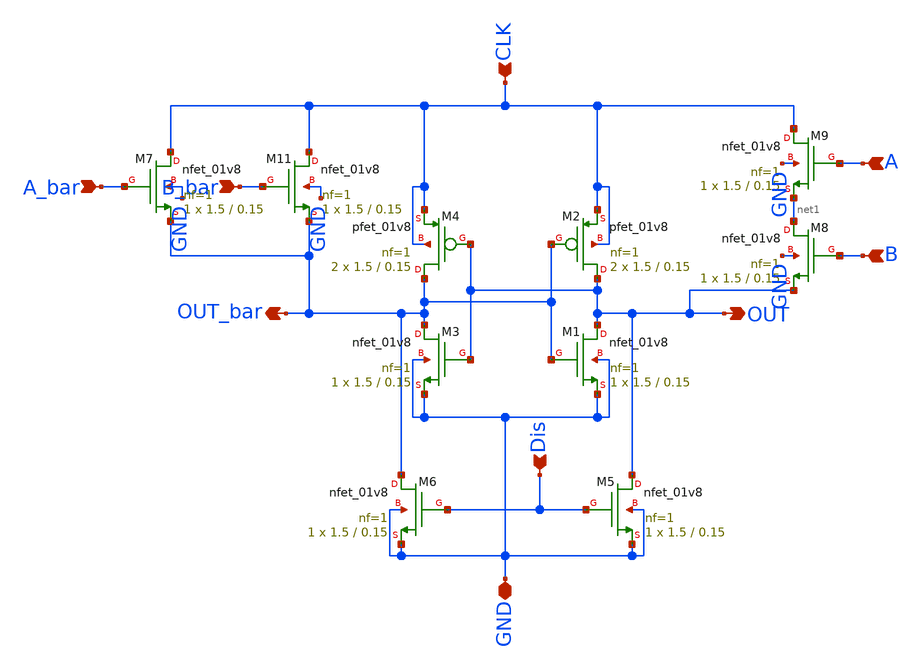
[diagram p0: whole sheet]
** sch_path: skywater_stuff/EESPFAL_NAND_v3_magic_checked.sch
**.subckt EESPFAL_NAND_v3_magic_checked A A_bar B B_bar OUT OUT_bar Dis GND CLK
*.ipin A
*.ipin A_bar
*.ipin B
*.ipin B_bar
*.opin OUT
*.opin OUT_bar
*.ipin Dis
*.iopin GND
*.ipin CLK
XM6 OUT_bar Dis GND GND sky130_fd_pr__nfet_01v8 L=0.15 W=1.5 nf=1 ad='int((nf+1)/2) * W/nf * 0.29' as='int((nf+2)/2) * W/nf * 0.29'
+ pd='2*int((nf+1)/2) * (W/nf + 0.29)' ps='2*int((nf+2)/2) * (W/nf + 0.29)' nrd='0.29 / W' nrs='0.29 / W'
+ sa=0 sb=0 sd=0 mult=1 m=1
XM9 CLK A net1 GND sky130_fd_pr__nfet_01v8 L=0.15 W=1.5 nf=1 ad='int((nf+1)/2) * W/nf * 0.29' as='int((nf+2)/2) * W/nf * 0.29'
+ pd='2*int((nf+1)/2) * (W/nf + 0.29)' ps='2*int((nf+2)/2) * (W/nf + 0.29)' nrd='0.29 / W' nrs='0.29 / W'
+ sa=0 sb=0 sd=0 mult=1 m=1
XM4 OUT_bar OUT CLK CLK sky130_fd_pr__pfet_01v8 L=0.15 W=1.5 nf=1 ad='int((nf+1)/2) * W/nf * 0.29' as='int((nf+2)/2) * W/nf * 0.29'
+ pd='2*int((nf+1)/2) * (W/nf + 0.29)' ps='2*int((nf+2)/2) * (W/nf + 0.29)' nrd='0.29 / W' nrs='0.29 / W'
+ sa=0 sb=0 sd=0 mult=2 m=2
XM3 OUT_bar OUT GND GND sky130_fd_pr__nfet_01v8 L=0.15 W=1.5 nf=1 ad='int((nf+1)/2) * W/nf * 0.29' as='int((nf+2)/2) * W/nf * 0.29'
+ pd='2*int((nf+1)/2) * (W/nf + 0.29)' ps='2*int((nf+2)/2) * (W/nf + 0.29)' nrd='0.29 / W' nrs='0.29 / W'
+ sa=0 sb=0 sd=0 mult=1 m=1
XM2 OUT OUT_bar CLK CLK sky130_fd_pr__pfet_01v8 L=0.15 W=1.5 nf=1 ad='int((nf+1)/2) * W/nf * 0.29' as='int((nf+2)/2) * W/nf * 0.29'
+ pd='2*int((nf+1)/2) * (W/nf + 0.29)' ps='2*int((nf+2)/2) * (W/nf + 0.29)' nrd='0.29 / W' nrs='0.29 / W'
+ sa=0 sb=0 sd=0 mult=2 m=2
XM11 CLK B_bar OUT_bar GND sky130_fd_pr__nfet_01v8 L=0.15 W=1.5 nf=1 ad='int((nf+1)/2) * W/nf * 0.29'
+ as='int((nf+2)/2) * W/nf * 0.29' pd='2*int((nf+1)/2) * (W/nf + 0.29)' ps='2*int((nf+2)/2) * (W/nf + 0.29)'
+ nrd='0.29 / W' nrs='0.29 / W' sa=0 sb=0 sd=0 mult=1 m=1
XM7 CLK A_bar OUT_bar GND sky130_fd_pr__nfet_01v8 L=0.15 W=1.5 nf=1 ad='int((nf+1)/2) * W/nf * 0.29'
+ as='int((nf+2)/2) * W/nf * 0.29' pd='2*int((nf+1)/2) * (W/nf + 0.29)' ps='2*int((nf+2)/2) * (W/nf + 0.29)'
+ nrd='0.29 / W' nrs='0.29 / W' sa=0 sb=0 sd=0 mult=1 m=1
XM8 net1 B OUT GND sky130_fd_pr__nfet_01v8 L=0.15 W=1.5 nf=1 ad='int((nf+1)/2) * W/nf * 0.29' as='int((nf+2)/2) * W/nf * 0.29'
+ pd='2*int((nf+1)/2) * (W/nf + 0.29)' ps='2*int((nf+2)/2) * (W/nf + 0.29)' nrd='0.29 / W' nrs='0.29 / W'
+ sa=0 sb=0 sd=0 mult=1 m=1
XM1 OUT OUT_bar GND GND sky130_fd_pr__nfet_01v8 L=0.15 W=1.5 nf=1 ad='int((nf+1)/2) * W/nf * 0.29' as='int((nf+2)/2) * W/nf * 0.29'
+ pd='2*int((nf+1)/2) * (W/nf + 0.29)' ps='2*int((nf+2)/2) * (W/nf + 0.29)' nrd='0.29 / W' nrs='0.29 / W'
+ sa=0 sb=0 sd=0 mult=1 m=1
XM5 OUT Dis GND GND sky130_fd_pr__nfet_01v8 L=0.15 W=1.5 nf=1 ad='int((nf+1)/2) * W/nf * 0.29' as='int((nf+2)/2) * W/nf * 0.29'
+ pd='2*int((nf+1)/2) * (W/nf + 0.29)' ps='2*int((nf+2)/2) * (W/nf + 0.29)' nrd='0.29 / W' nrs='0.29 / W'
+ sa=0 sb=0 sd=0 mult=1 m=1
**.ends
.end
